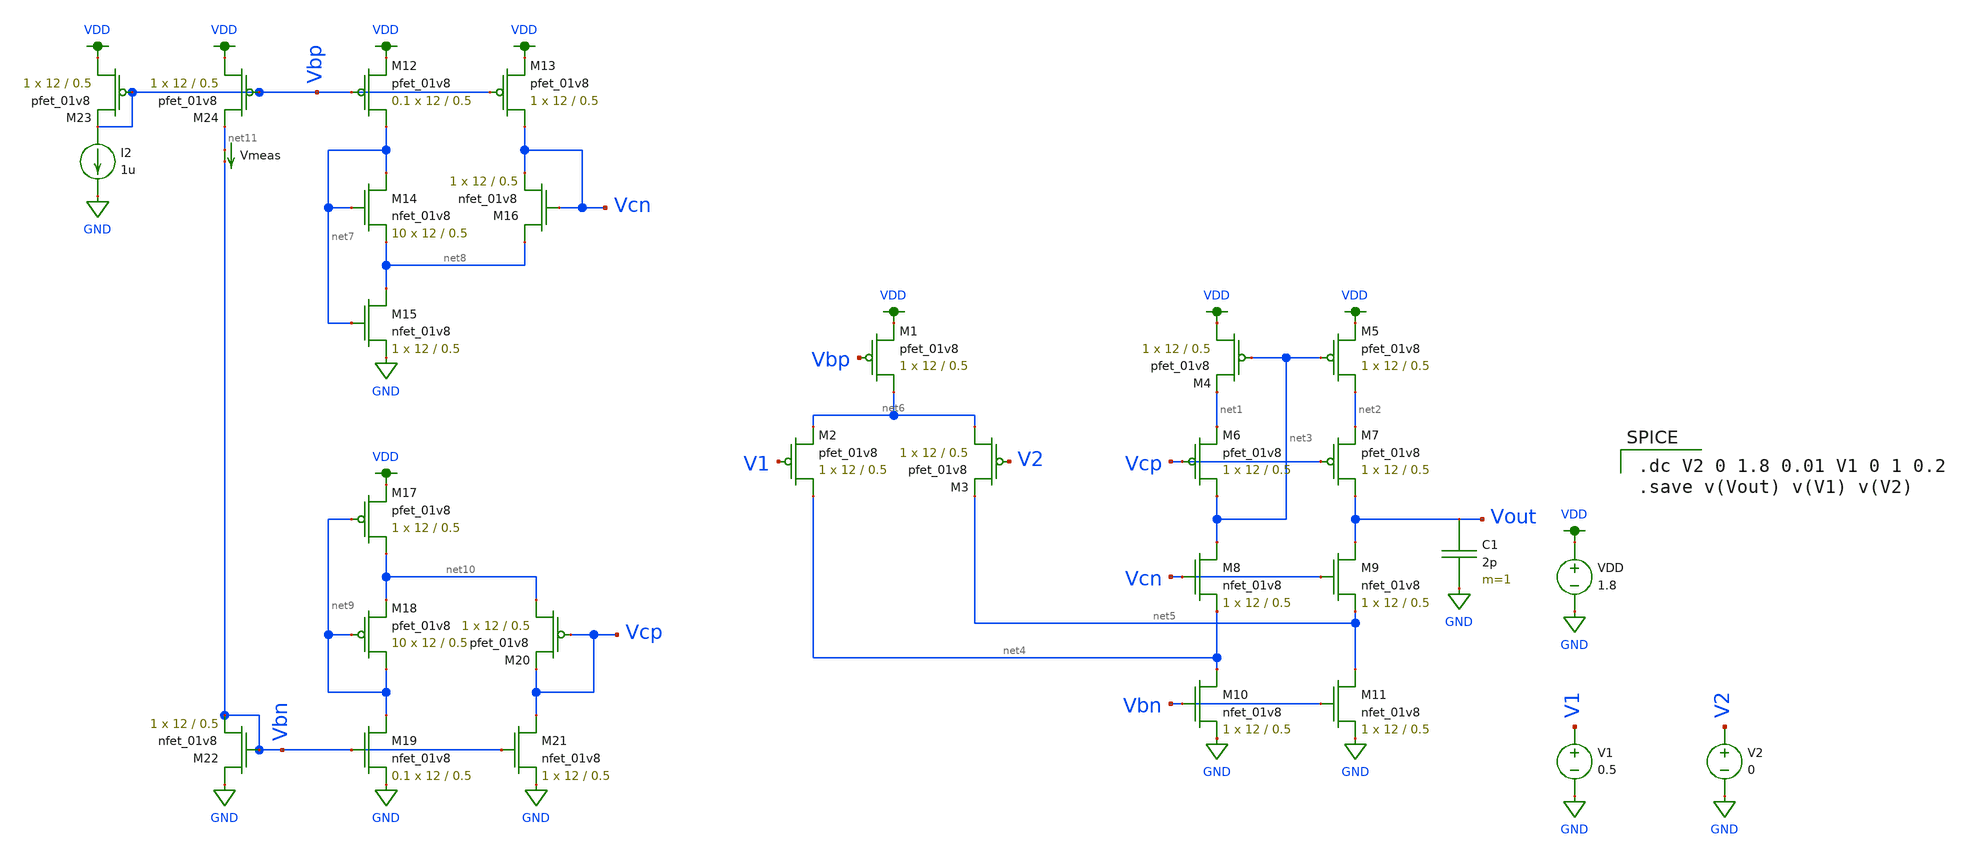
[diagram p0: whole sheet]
** sch_path: schematic/folded_cascode_differential_amplifier.sch
**.subckt folded_cascode_differential_amplifier
XM1 net6 Vbp VDD VDD sky130_fd_pr__pfet_01v8 L=0.5 W=12 nf=1 ad='int((nf+1)/2) * W/nf * 0.29' as='int((nf+2)/2) * W/nf * 0.29'
+ pd='2*int((nf+1)/2) * (W/nf + 0.29)' ps='2*int((nf+2)/2) * (W/nf + 0.29)' nrd='0.29 / W' nrs='0.29 / W'
+ sa=0 sb=0 sd=0 mult=1 m=1
XM2 net4 V1 net6 VDD sky130_fd_pr__pfet_01v8 L=0.5 W=12 nf=1 ad='int((nf+1)/2) * W/nf * 0.29' as='int((nf+2)/2) * W/nf * 0.29'
+ pd='2*int((nf+1)/2) * (W/nf + 0.29)' ps='2*int((nf+2)/2) * (W/nf + 0.29)' nrd='0.29 / W' nrs='0.29 / W'
+ sa=0 sb=0 sd=0 mult=1 m=1
XM3 net6 V2 net5 VDD sky130_fd_pr__pfet_01v8 L=0.5 W=12 nf=1 ad='int((nf+1)/2) * W/nf * 0.29' as='int((nf+2)/2) * W/nf * 0.29'
+ pd='2*int((nf+1)/2) * (W/nf + 0.29)' ps='2*int((nf+2)/2) * (W/nf + 0.29)' nrd='0.29 / W' nrs='0.29 / W'
+ sa=0 sb=0 sd=0 mult=1 m=1
XM4 VDD net3 net1 VDD sky130_fd_pr__pfet_01v8 L=0.5 W=12 nf=1 ad='int((nf+1)/2) * W/nf * 0.29' as='int((nf+2)/2) * W/nf * 0.29'
+ pd='2*int((nf+1)/2) * (W/nf + 0.29)' ps='2*int((nf+2)/2) * (W/nf + 0.29)' nrd='0.29 / W' nrs='0.29 / W'
+ sa=0 sb=0 sd=0 mult=1 m=1
XM5 net2 net3 VDD VDD sky130_fd_pr__pfet_01v8 L=0.5 W=12 nf=1 ad='int((nf+1)/2) * W/nf * 0.29' as='int((nf+2)/2) * W/nf * 0.29'
+ pd='2*int((nf+1)/2) * (W/nf + 0.29)' ps='2*int((nf+2)/2) * (W/nf + 0.29)' nrd='0.29 / W' nrs='0.29 / W'
+ sa=0 sb=0 sd=0 mult=1 m=1
XM6 net3 Vcp net1 VDD sky130_fd_pr__pfet_01v8 L=0.5 W=12 nf=1 ad='int((nf+1)/2) * W/nf * 0.29' as='int((nf+2)/2) * W/nf * 0.29'
+ pd='2*int((nf+1)/2) * (W/nf + 0.29)' ps='2*int((nf+2)/2) * (W/nf + 0.29)' nrd='0.29 / W' nrs='0.29 / W'
+ sa=0 sb=0 sd=0 mult=1 m=1
XM7 Vout Vcp net2 VDD sky130_fd_pr__pfet_01v8 L=0.5 W=12 nf=1 ad='int((nf+1)/2) * W/nf * 0.29' as='int((nf+2)/2) * W/nf * 0.29'
+ pd='2*int((nf+1)/2) * (W/nf + 0.29)' ps='2*int((nf+2)/2) * (W/nf + 0.29)' nrd='0.29 / W' nrs='0.29 / W'
+ sa=0 sb=0 sd=0 mult=1 m=1
XM8 net3 Vcn net4 GND sky130_fd_pr__nfet_01v8 L=0.5 W=12 nf=1 ad='int((nf+1)/2) * W/nf * 0.29' as='int((nf+2)/2) * W/nf * 0.29'
+ pd='2*int((nf+1)/2) * (W/nf + 0.29)' ps='2*int((nf+2)/2) * (W/nf + 0.29)' nrd='0.29 / W' nrs='0.29 / W'
+ sa=0 sb=0 sd=0 mult=1 m=1
XM9 Vout Vcn net5 GND sky130_fd_pr__nfet_01v8 L=0.5 W=12 nf=1 ad='int((nf+1)/2) * W/nf * 0.29' as='int((nf+2)/2) * W/nf * 0.29'
+ pd='2*int((nf+1)/2) * (W/nf + 0.29)' ps='2*int((nf+2)/2) * (W/nf + 0.29)' nrd='0.29 / W' nrs='0.29 / W'
+ sa=0 sb=0 sd=0 mult=1 m=1
XM10 net4 Vbn GND GND sky130_fd_pr__nfet_01v8 L=0.5 W=12 nf=1 ad='int((nf+1)/2) * W/nf * 0.29' as='int((nf+2)/2) * W/nf * 0.29'
+ pd='2*int((nf+1)/2) * (W/nf + 0.29)' ps='2*int((nf+2)/2) * (W/nf + 0.29)' nrd='0.29 / W' nrs='0.29 / W'
+ sa=0 sb=0 sd=0 mult=1 m=1
XM11 net5 Vbn GND GND sky130_fd_pr__nfet_01v8 L=0.5 W=12 nf=1 ad='int((nf+1)/2) * W/nf * 0.29' as='int((nf+2)/2) * W/nf * 0.29'
+ pd='2*int((nf+1)/2) * (W/nf + 0.29)' ps='2*int((nf+2)/2) * (W/nf + 0.29)' nrd='0.29 / W' nrs='0.29 / W'
+ sa=0 sb=0 sd=0 mult=1 m=1
XM12 net7 Vbp VDD VDD sky130_fd_pr__pfet_01v8 L=0.5 W=12 nf=1 ad='int((nf+1)/2) * W/nf * 0.29' as='int((nf+2)/2) * W/nf * 0.29'
+ pd='2*int((nf+1)/2) * (W/nf + 0.29)' ps='2*int((nf+2)/2) * (W/nf + 0.29)' nrd='0.29 / W' nrs='0.29 / W'
+ sa=0 sb=0 sd=0 mult=0.1 m=0.1
XM13 Vcn Vbp VDD VDD sky130_fd_pr__pfet_01v8 L=0.5 W=12 nf=1 ad='int((nf+1)/2) * W/nf * 0.29' as='int((nf+2)/2) * W/nf * 0.29'
+ pd='2*int((nf+1)/2) * (W/nf + 0.29)' ps='2*int((nf+2)/2) * (W/nf + 0.29)' nrd='0.29 / W' nrs='0.29 / W'
+ sa=0 sb=0 sd=0 mult=1 m=1
XM14 net7 net7 net8 GND sky130_fd_pr__nfet_01v8 L=0.5 W=12 nf=1 ad='int((nf+1)/2) * W/nf * 0.29' as='int((nf+2)/2) * W/nf * 0.29'
+ pd='2*int((nf+1)/2) * (W/nf + 0.29)' ps='2*int((nf+2)/2) * (W/nf + 0.29)' nrd='0.29 / W' nrs='0.29 / W'
+ sa=0 sb=0 sd=0 mult=10 m=10
XM15 net8 net7 GND GND sky130_fd_pr__nfet_01v8 L=0.5 W=12 nf=1 ad='int((nf+1)/2) * W/nf * 0.29' as='int((nf+2)/2) * W/nf * 0.29'
+ pd='2*int((nf+1)/2) * (W/nf + 0.29)' ps='2*int((nf+2)/2) * (W/nf + 0.29)' nrd='0.29 / W' nrs='0.29 / W'
+ sa=0 sb=0 sd=0 mult=1 m=1
XM16 net8 Vcn Vcn GND sky130_fd_pr__nfet_01v8 L=0.5 W=12 nf=1 ad='int((nf+1)/2) * W/nf * 0.29' as='int((nf+2)/2) * W/nf * 0.29'
+ pd='2*int((nf+1)/2) * (W/nf + 0.29)' ps='2*int((nf+2)/2) * (W/nf + 0.29)' nrd='0.29 / W' nrs='0.29 / W'
+ sa=0 sb=0 sd=0 mult=1 m=1
XM17 net10 net9 VDD VDD sky130_fd_pr__pfet_01v8 L=0.5 W=12 nf=1 ad='int((nf+1)/2) * W/nf * 0.29' as='int((nf+2)/2) * W/nf * 0.29'
+ pd='2*int((nf+1)/2) * (W/nf + 0.29)' ps='2*int((nf+2)/2) * (W/nf + 0.29)' nrd='0.29 / W' nrs='0.29 / W'
+ sa=0 sb=0 sd=0 mult=1 m=1
XM18 net9 net9 net10 VDD sky130_fd_pr__pfet_01v8 L=0.5 W=12 nf=1 ad='int((nf+1)/2) * W/nf * 0.29' as='int((nf+2)/2) * W/nf * 0.29'
+ pd='2*int((nf+1)/2) * (W/nf + 0.29)' ps='2*int((nf+2)/2) * (W/nf + 0.29)' nrd='0.29 / W' nrs='0.29 / W'
+ sa=0 sb=0 sd=0 mult=10 m=10
XM19 net9 Vbn GND GND sky130_fd_pr__nfet_01v8 L=0.5 W=12 nf=1 ad='int((nf+1)/2) * W/nf * 0.29' as='int((nf+2)/2) * W/nf * 0.29'
+ pd='2*int((nf+1)/2) * (W/nf + 0.29)' ps='2*int((nf+2)/2) * (W/nf + 0.29)' nrd='0.29 / W' nrs='0.29 / W'
+ sa=0 sb=0 sd=0 mult=0.1 m=0.1
XM20 net10 Vcp Vcp VDD sky130_fd_pr__pfet_01v8 L=0.5 W=12 nf=1 ad='int((nf+1)/2) * W/nf * 0.29' as='int((nf+2)/2) * W/nf * 0.29'
+ pd='2*int((nf+1)/2) * (W/nf + 0.29)' ps='2*int((nf+2)/2) * (W/nf + 0.29)' nrd='0.29 / W' nrs='0.29 / W'
+ sa=0 sb=0 sd=0 mult=1 m=1
XM21 Vcp Vbn GND GND sky130_fd_pr__nfet_01v8 L=0.5 W=12 nf=1 ad='int((nf+1)/2) * W/nf * 0.29' as='int((nf+2)/2) * W/nf * 0.29'
+ pd='2*int((nf+1)/2) * (W/nf + 0.29)' ps='2*int((nf+2)/2) * (W/nf + 0.29)' nrd='0.29 / W' nrs='0.29 / W'
+ sa=0 sb=0 sd=0 mult=1 m=1
VDD VDD GND 1.8
V1 V1 GND 0.5
C1 Vout GND 2p m=1
V2 V2 GND 0
XM22 GND Vbn Vbn GND sky130_fd_pr__nfet_01v8 L=0.5 W=12 nf=1 ad='int((nf+1)/2) * W/nf * 0.29' as='int((nf+2)/2) * W/nf * 0.29'
+ pd='2*int((nf+1)/2) * (W/nf + 0.29)' ps='2*int((nf+2)/2) * (W/nf + 0.29)' nrd='0.29 / W' nrs='0.29 / W'
+ sa=0 sb=0 sd=0 mult=1 m=1
XM23 VDD Vbp Vbp VDD sky130_fd_pr__pfet_01v8 L=0.5 W=12 nf=1 ad='int((nf+1)/2) * W/nf * 0.29' as='int((nf+2)/2) * W/nf * 0.29'
+ pd='2*int((nf+1)/2) * (W/nf + 0.29)' ps='2*int((nf+2)/2) * (W/nf + 0.29)' nrd='0.29 / W' nrs='0.29 / W'
+ sa=0 sb=0 sd=0 mult=1 m=1
I2 Vbp GND 1u
XM24 VDD Vbp net11 VDD sky130_fd_pr__pfet_01v8 L=0.5 W=12 nf=1 ad='int((nf+1)/2) * W/nf * 0.29' as='int((nf+2)/2) * W/nf * 0.29'
+ pd='2*int((nf+1)/2) * (W/nf + 0.29)' ps='2*int((nf+2)/2) * (W/nf + 0.29)' nrd='0.29 / W' nrs='0.29 / W'
+ sa=0 sb=0 sd=0 mult=1 m=1
Vmeas net11 Vbn 0
.save i(vmeas)
**** begin user architecture code

.option wnflag=1
.lib ~/skywater/skywater-pdk/libraries/sky130_fd_pr_ngspice/latest/models/sky130.lib.spice tt


.dc V2 0 1.8 0.01 V1 0 1 0.2
.save v(Vout) v(V1) v(V2)

**** end user architecture code
**.ends
.GLOBAL VDD
.GLOBAL GND
.end
